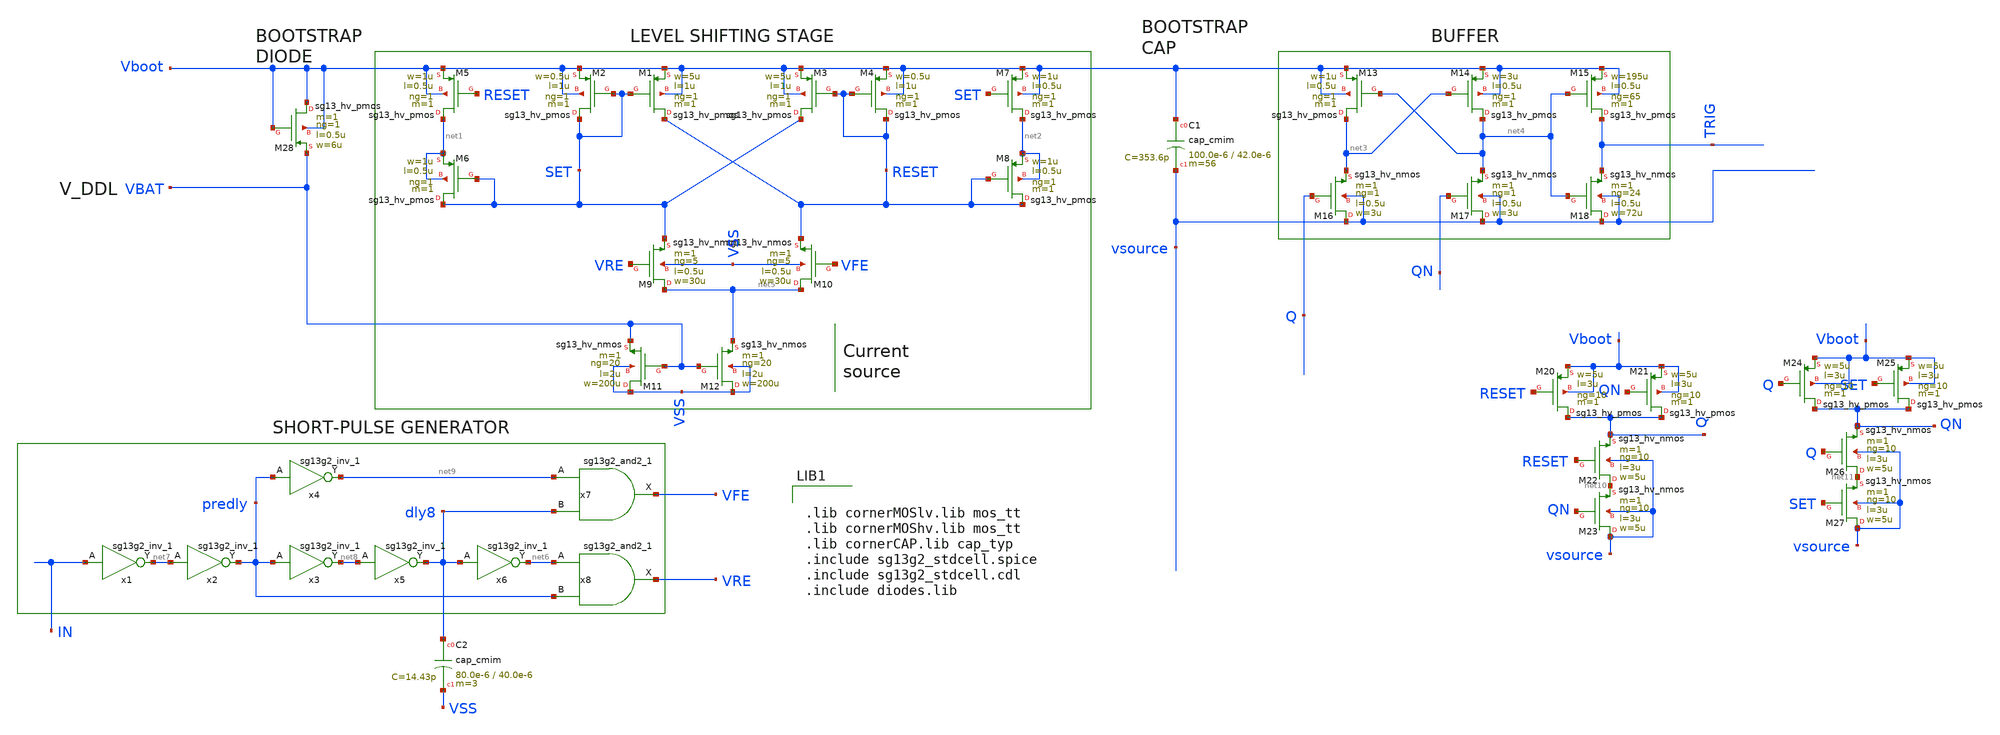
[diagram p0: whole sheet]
** sch_path: xschem/Floating_Gate/Full_Gate_Driver.sch
**.subckt Full_Gate_Driver
XM1 RESET SET Vboot Vboot sg13_hv_pmos w=5u l=1u ng=1 m=1 mm_ok=1
XM2 SET SET Vboot Vboot sg13_hv_pmos w=0.5u l=1u ng=1 m=1 mm_ok=1
XM3 SET RESET Vboot Vboot sg13_hv_pmos w=5u l=1u ng=1 m=1 mm_ok=1
XM4 RESET RESET Vboot Vboot sg13_hv_pmos w=0.5u l=1u ng=1 m=1 mm_ok=1
XM5 net1 RESET Vboot Vboot sg13_hv_pmos w=1u l=0.5u ng=1 m=1 mm_ok=1
XM6 SET SET net1 net1 sg13_hv_pmos w=1u l=0.5u ng=1 m=1 mm_ok=1
XM7 net2 SET Vboot Vboot sg13_hv_pmos w=1u l=0.5u ng=1 m=1 mm_ok=1
XM8 RESET RESET net2 net2 sg13_hv_pmos w=1u l=0.5u ng=1 m=1 mm_ok=1
XM9 net5 VRE SET VSS sg13_hv_nmos w=30u l=0.5u ng=5 m=1 mm_ok=1
XM10 net5 VFE RESET VSS sg13_hv_nmos w=30u l=0.5u ng=5 m=1 mm_ok=1
XM11 VSS VBAT VBAT VSS sg13_hv_nmos w=200u l=2u ng=20 m=1 mm_ok=1
XM12 VSS VBAT net5 VSS sg13_hv_nmos w=200u l=2u ng=20 m=1 mm_ok=1
XM13 net3 net4 Vboot Vboot sg13_hv_pmos w=1u l=0.5u ng=1 m=1 mm_ok=1
XM14 net4 net3 Vboot Vboot sg13_hv_pmos w=3u l=0.5u ng=1 m=1 mm_ok=1
XM15 TRIG net4 Vboot Vboot sg13_hv_pmos w=195u l=0.5u ng=65 m=1 mm_ok=1
XM16 vsource Q net3 vsource sg13_hv_nmos w=3u l=0.5u ng=1 m=1 mm_ok=1
XM17 vsource QN net4 vsource sg13_hv_nmos w=3u l=0.5u ng=1 m=1 mm_ok=1
XM18 vsource net4 TRIG vsource sg13_hv_nmos w=72u l=0.5u ng=24 m=1 mm_ok=1
XM20 Q RESET Vboot Vboot sg13_hv_pmos w=5u l=3u ng=10 m=1 mm_ok=1
XM21 Q QN Vboot Vboot sg13_hv_pmos w=5u l=3u ng=10 m=1 mm_ok=1
XM22 net10 RESET Q vsource sg13_hv_nmos w=5u l=3u ng=10 m=1 mm_ok=1
XM23 vsource QN net10 vsource sg13_hv_nmos w=5u l=3u ng=10 m=1 mm_ok=1
XM24 QN Q Vboot Vboot sg13_hv_pmos w=5u l=3u ng=10 m=1 mm_ok=1
XM25 QN SET Vboot Vboot sg13_hv_pmos w=5u l=3u ng=10 m=1 mm_ok=1
XM26 net11 Q QN vsource sg13_hv_nmos w=5u l=3u ng=10 m=1 mm_ok=1
XM27 vsource SET net11 vsource sg13_hv_nmos w=5u l=3u ng=10 m=1 mm_ok=1
x1 net7 IN VDD VSS sg13g2_inv_1
x2 predly net7 VDD VSS sg13g2_inv_1
x3 net8 predly VDD VSS sg13g2_inv_1
x4 net9 predly VDD VSS sg13g2_inv_1
x5 dly8 net8 VDD VSS sg13g2_inv_1
x6 net6 dly8 VDD VSS sg13g2_inv_1
x7 VFE net9 dly8 VDD VSS sg13g2_and2_1
x8 VRE net6 predly VDD VSS sg13g2_and2_1
XC2 dly8 VSS cap_cmim w=80.0e-6 l=40.0e-6 m=3 mm_ok=1
XC1 Vboot vsource cap_cmim w=100.0e-6 l=42.0e-6 m=56 mm_ok=1
XM28 Vboot Vboot VBAT Vboot sg13_hv_pmos w=6u l=0.5u ng=1 m=1 mm_ok=1
**** begin user architecture code


.lib cornerMOSlv.lib mos_tt
.lib cornerMOShv.lib mos_tt
.lib cornerCAP.lib cap_typ
.include sg13g2_stdcell.spice
.include sg13g2_stdcell.cdl
.include diodes.lib


**** end user architecture code
**.ends

* expanding   symbol:  sg13g2_stdcells/sg13g2_inv_1.sym # of pins=2
** sym_path: sg13g2_stdcells/sg13g2_inv_1.sym
** sch_path: sg13g2_stdcells/sg13g2_inv_1.sch
.subckt sg13g2_inv_1 Y A VDD VSS
*.opin Y
*.ipin A
*.iopin VDD
*.iopin VSS
XM1 Y A VSS VSS sg13_lv_nmos w=740.00n l=130.00n ng=1 m=1 mm_ok=1
XM2 Y A VDD VDD sg13_lv_pmos w=1.12u l=130.00n ng=1 m=1 mm_ok=1
.ends


* expanding   symbol:  sg13g2_stdcells/sg13g2_and2_1.sym # of pins=3
** sym_path: sg13g2_stdcells/sg13g2_and2_1.sym
** sch_path: sg13g2_stdcells/sg13g2_and2_1.sch
.subckt sg13g2_and2_1 X A B VDD VSS
*.ipin A
*.ipin B
*.opin X
*.iopin VDD
*.iopin VSS
XM1 net1 A net2 VSS sg13_lv_nmos w=640.00n l=130.00n ng=1 m=1 mm_ok=1
XM2 net2 B VSS VSS sg13_lv_nmos w=640.00n l=130.00n ng=1 m=1 mm_ok=1
XM3 X net1 VSS VSS sg13_lv_nmos w=740.00n l=130.00n ng=1 m=1 mm_ok=1
XM4 net1 B VDD VDD sg13_lv_pmos w=840.00n l=130.00n ng=1 m=1 mm_ok=1
XM5 net1 A VDD VDD sg13_lv_pmos w=840.00n l=130.00n ng=1 m=1 mm_ok=1
XM6 X net1 VDD VDD sg13_lv_pmos w=1.12u l=130.00n ng=1 m=1 mm_ok=1
.ends

.end
